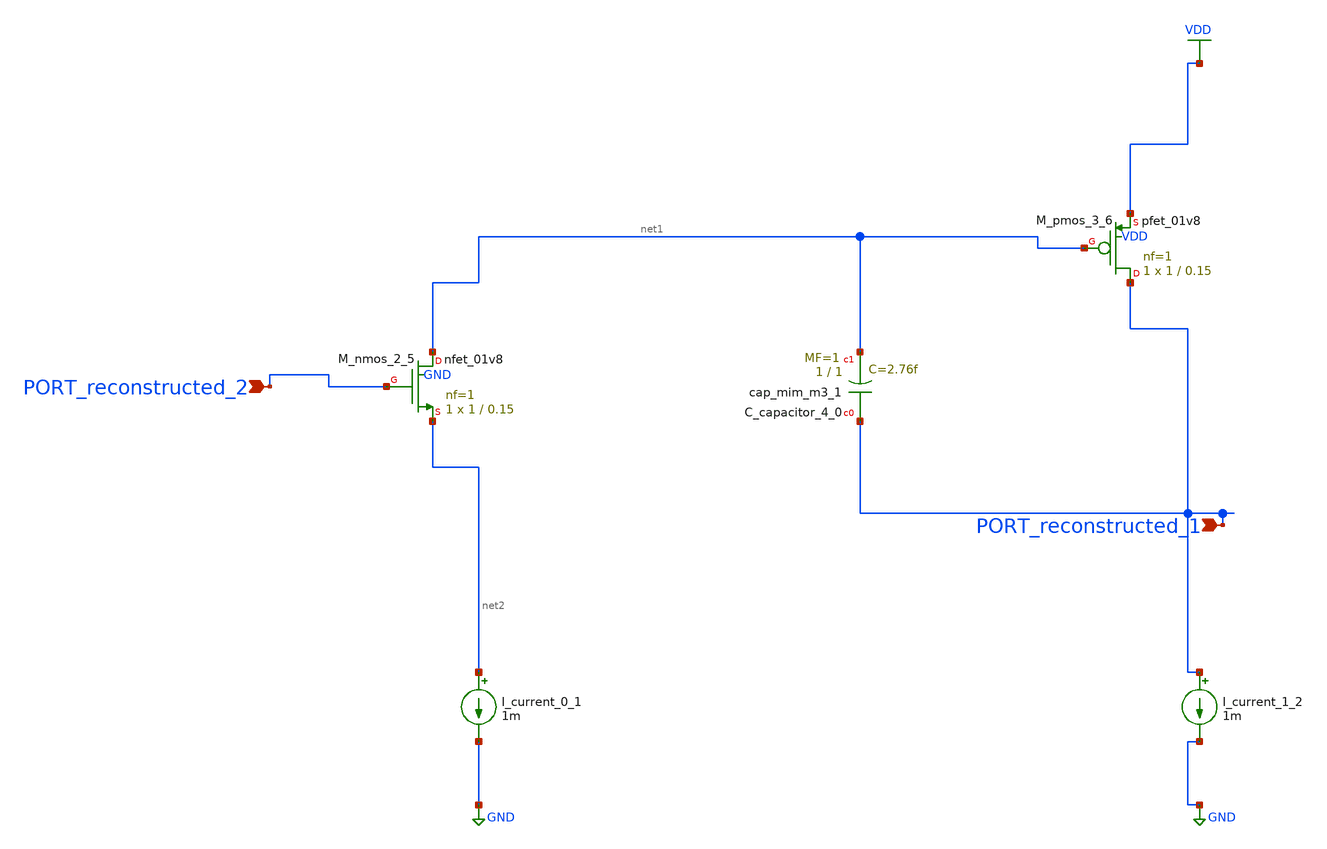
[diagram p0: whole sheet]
** sch_path: schematics/AMSNet/729.sch
**.subckt 729 PORT_reconstructed_2 PORT_reconstructed_1
*.ipin PORT_reconstructed_2
*.ipin PORT_reconstructed_1
XC_capacitor_4_0 PORT_reconstructed_1 net1 sky130_fd_pr__cap_mim_m3_1 W=1 L=1 MF=1 m=1
I_current_0_1 net2 GND 1m
I_current_1_2 PORT_reconstructed_1 GND 1m
XM_nmos_2_5 net1 PORT_reconstructed_2 net2 GND sky130_fd_pr__nfet_01v8 L=0.15 W=1 nf=1 ad='int((1 + 1)/2) * 1 / 1 * 0.29'
+ as='int((1 + 2)/2) * 1 / 1 * 0.29' pd='2*int((1 + 1)/2) * (1 / 1 + 0.29)' ps='2*int((1 + 2)/2) * (1 / 1 + 0.29)'
+ nrd='0.29 / 1 ' nrs='0.29 / 1 ' sa=0 sb=0 sd=0 mult=1 m=1
XM_pmos_3_6 PORT_reconstructed_1 net1 VDD VDD sky130_fd_pr__pfet_01v8 L=0.15 W=1 nf=1 ad='int((1 + 1)/2) * 1 / 1 * 0.29'
+ as='int((1 + 2)/2) * 1 / 1 * 0.29' pd='2*int((1 + 1)/2) * (1 / 1 + 0.29)' ps='2*int((1 + 2)/2) * (1 / 1 + 0.29)'
+ nrd='0.29 / 1 ' nrs='0.29 / 1 ' sa=0 sb=0 sd=0 mult=1 m=1
**.ends
.GLOBAL GND
.GLOBAL VDD
.end
